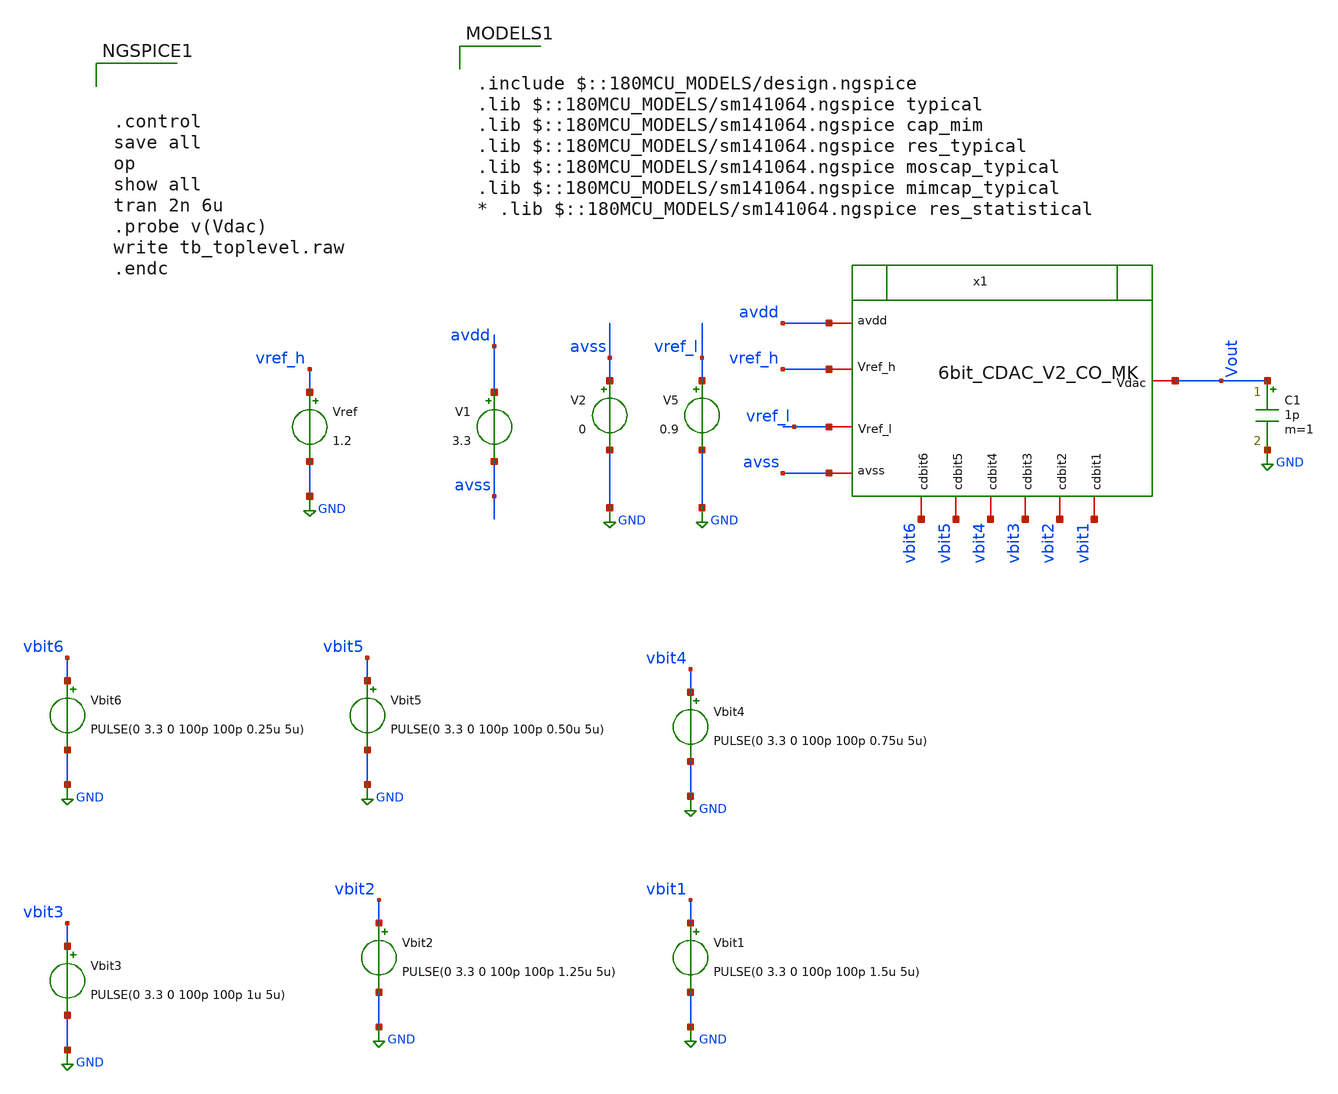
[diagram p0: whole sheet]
** sch_path: designs/full_ADC/tb_toplevel.sch
**.subckt tb_toplevel
V1 avdd avss 3.3
V2 avss GND 0
Vbit1 vbit1 GND PULSE(0 3.3 0 100p 100p 1.5u 5u)
Vbit2 vbit2 GND PULSE(0 3.3 0 100p 100p 1.25u 5u)
Vbit3 vbit3 GND PULSE(0 3.3 0 100p 100p 1u 5u)
Vbit4 vbit4 GND PULSE(0 3.3 0 100p 100p 0.75u 5u)
Vbit5 vbit5 GND PULSE(0 3.3 0 100p 100p 0.50u 5u)
Vbit6 vbit6 GND PULSE(0 3.3 0 100p 100p 0.25u 5u)
Vref vref_h GND 1.2
C1 Vout GND 1p m=1
x1 vref_l Vout avdd avss vref_h vbit6 vbit5 vbit3 vbit1 vbit2 vbit4 6bit_CDAC_V2_CO_MK
V5 vref_l GND 0.9
**** begin user architecture code



.control
save all
op
show all
tran 2n 6u
.probe v(Vdac)
write tb_toplevel.raw
.endc



.include $::180MCU_MODELS/design.ngspice
.lib $::180MCU_MODELS/sm141064.ngspice typical
.lib $::180MCU_MODELS/sm141064.ngspice cap_mim
.lib $::180MCU_MODELS/sm141064.ngspice res_typical
.lib $::180MCU_MODELS/sm141064.ngspice moscap_typical
.lib $::180MCU_MODELS/sm141064.ngspice mimcap_typical
* .lib $::180MCU_MODELS/sm141064.ngspice res_statistical

**** end user architecture code
**.ends
.GLOBAL GND
.end
